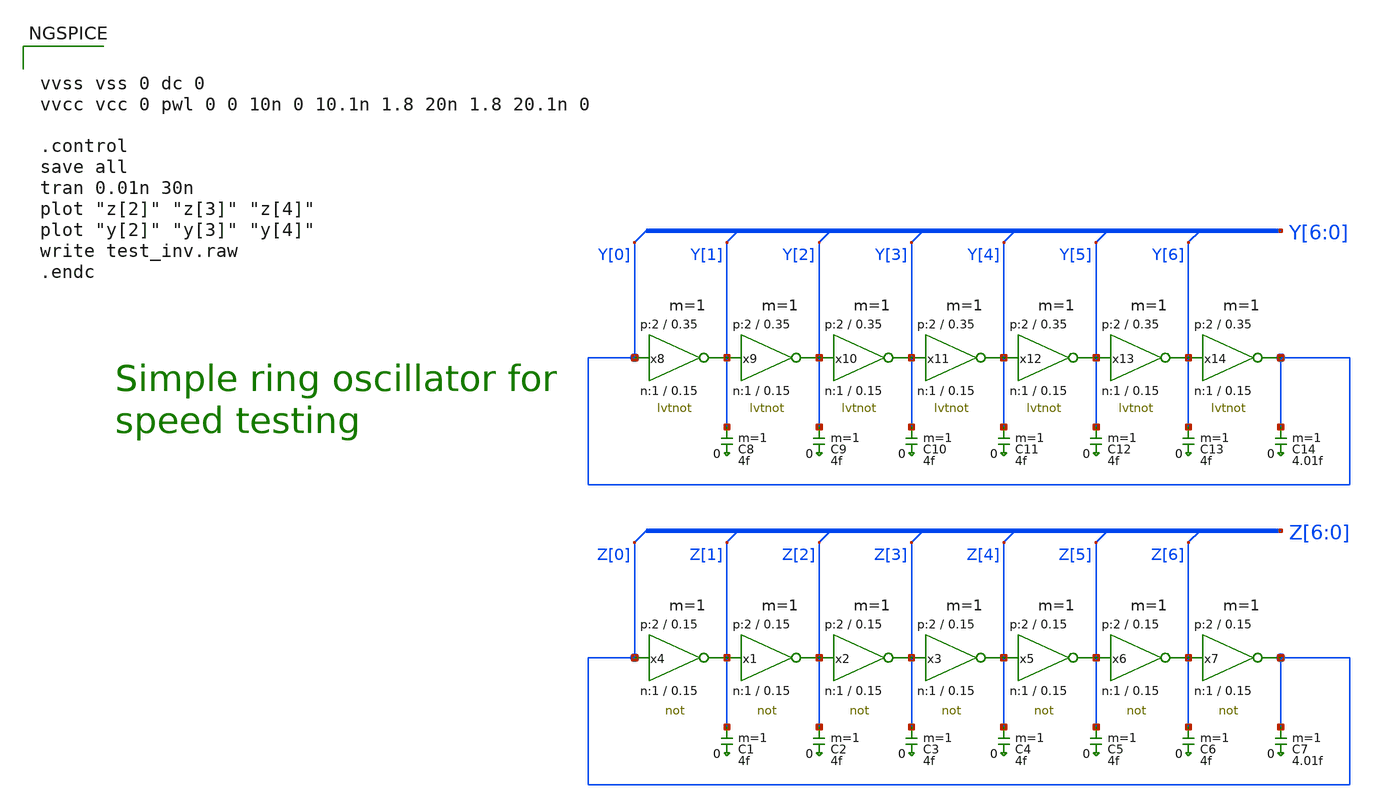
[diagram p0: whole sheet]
** sch_path: sky130_tests/test_inv.sch
* Copyright 2021 Stefan Frederik Schippers
* Licensed under the Apache License, Version 2.0 (the "License");
* you may not use this file except in compliance with the License.
* You may obtain a copy of the License at
* https://www.apache.org/licenses/LICENSE-2.0
* Unless required by applicable law or agreed to in writing, software
* distributed under the License is distributed on an "AS IS" BASIS,
* WITHOUT WARRANTIES OR CONDITIONS OF ANY KIND, either express or implied.
* See the License for the specific language governing permissions and
* limitations under the License.
**.subckt test_inv
C1 Z[1] 0 4f m=1
C2 Z[2] 0 4f m=1
C3 Z[3] 0 4f m=1
C4 Z[4] 0 4f m=1
C5 Z[5] 0 4f m=1
C6 Z[6] 0 4f m=1
C7 Z[0] 0 4.01f m=1
C8 Y[1] 0 4f m=1
C9 Y[2] 0 4f m=1
C10 Y[3] 0 4f m=1
C11 Y[4] 0 4f m=1
C12 Y[5] 0 4f m=1
C13 Y[6] 0 4f m=1
C14 Y[0] 0 4.01f m=1
x4 Z[1] Z[0] VCC VSS not W_N=1 L_N=0.15 W_P=2 L_P=0.15 m=1
x1 Z[2] Z[1] VCC VSS not W_N=1 L_N=0.15 W_P=2 L_P=0.15 m=1
x2 Z[3] Z[2] VCC VSS not W_N=1 L_N=0.15 W_P=2 L_P=0.15 m=1
x3 Z[4] Z[3] VCC VSS not W_N=1 L_N=0.15 W_P=2 L_P=0.15 m=1
x5 Z[5] Z[4] VCC VSS not W_N=1 L_N=0.15 W_P=2 L_P=0.15 m=1
x6 Z[6] Z[5] VCC VSS not W_N=1 L_N=0.15 W_P=2 L_P=0.15 m=1
x7 Z[0] Z[6] VCC VSS not W_N=1 L_N=0.15 W_P=2 L_P=0.15 m=1
x8 Y[0] Y[1] VCC VSS lvtnot W_N=1 L_N=0.15 W_P=2 L_P=0.35 m=1
x9 Y[1] Y[2] VCC VSS lvtnot W_N=1 L_N=0.15 W_P=2 L_P=0.35 m=1
x10 Y[2] Y[3] VCC VSS lvtnot W_N=1 L_N=0.15 W_P=2 L_P=0.35 m=1
x11 Y[3] Y[4] VCC VSS lvtnot W_N=1 L_N=0.15 W_P=2 L_P=0.35 m=1
x12 Y[4] Y[5] VCC VSS lvtnot W_N=1 L_N=0.15 W_P=2 L_P=0.35 m=1
x13 Y[5] Y[6] VCC VSS lvtnot W_N=1 L_N=0.15 W_P=2 L_P=0.35 m=1
x14 Y[6] Y[0] VCC VSS lvtnot W_N=1 L_N=0.15 W_P=2 L_P=0.35 m=1
**** begin user architecture code


vvss vss 0 dc 0
vvcc vcc 0 pwl 0 0 10n 0 10.1n 1.8 20n 1.8 20.1n 0

.control
save all
tran 0.01n 30n
plot "z[2]" "z[3]" "z[4]"
plot "y[2]" "y[3]" "y[4]"
write test_inv.raw
.endc


 ** manual skywater pdks install (with patches applied)
* .lib $::SKYWATER_MODELS/models/sky130.lib.spice tt

** opencircuitdesign pdks install
.lib $::SKYWATER_MODELS/sky130.lib.spice tt

.param mc_mm_switch=0
.param mc_pr_switch=0

**** end user architecture code
**.ends

* expanding   symbol:  sky130_tests/not.sym # of pins=2
** sym_path: sky130_tests/not.sym
** sch_path: sky130_tests/not.sch
.subckt not y a VCCPIN VSSPIN     W_N=1 L_N=0.15 W_P=2 L_P=0.15
*.opin y
*.ipin a
XM1 y a VSSPIN VSSPIN sky130_fd_pr__nfet_01v8 L=L_N W=W_N nf=1 ad='int((nf+1)/2) * W/nf * 0.29' as='int((nf+2)/2) * W/nf * 0.29'
+ pd='2*int((nf+1)/2) * (W/nf + 0.29)' ps='2*int((nf+2)/2) * (W/nf + 0.29)' nrd='0.29 / W' nrs='0.29 / W'
+ sa=0 sb=0 sd=0 mult=1 m=1
XM2 y a VCCPIN VCCPIN sky130_fd_pr__pfet_01v8 L=L_P W=W_P nf=1 ad='int((nf+1)/2) * W/nf * 0.29' as='int((nf+2)/2) * W/nf * 0.29'
+ pd='2*int((nf+1)/2) * (W/nf + 0.29)' ps='2*int((nf+2)/2) * (W/nf + 0.29)' nrd='0.29 / W' nrs='0.29 / W'
+ sa=0 sb=0 sd=0 mult=1 m=1
.ends


* expanding   symbol:  sky130_tests/lvtnot.sym # of pins=2
** sym_path: sky130_tests/lvtnot.sym
** sch_path: sky130_tests/lvtnot.sch
.subckt lvtnot a y VCCPIN VSSPIN     W_N=1 L_N=0.15 W_P=2 L_P=0.35
*.opin y
*.ipin a
XM2 y a VCCPIN VCCPIN sky130_fd_pr__pfet_01v8_lvt L=L_P W=W_P nf=1 ad='int((nf+1)/2) * W/nf * 0.29' as='int((nf+2)/2) * W/nf * 0.29'
+ pd='2*int((nf+1)/2) * (W/nf + 0.29)' ps='2*int((nf+2)/2) * (W/nf + 0.29)' nrd='0.29 / W' nrs='0.29 / W'
+ sa=0 sb=0 sd=0 mult=1 m=1
XM1 y a VSSPIN VSSPIN sky130_fd_pr__nfet_01v8_lvt L=L_N W=W_N nf=1 ad='int((nf+1)/2) * W/nf * 0.29' as='int((nf+2)/2) * W/nf * 0.29'
+ pd='2*int((nf+1)/2) * (W/nf + 0.29)' ps='2*int((nf+2)/2) * (W/nf + 0.29)' nrd='0.29 / W' nrs='0.29 / W'
+ sa=0 sb=0 sd=0 mult=1 m=1
.ends

.end
